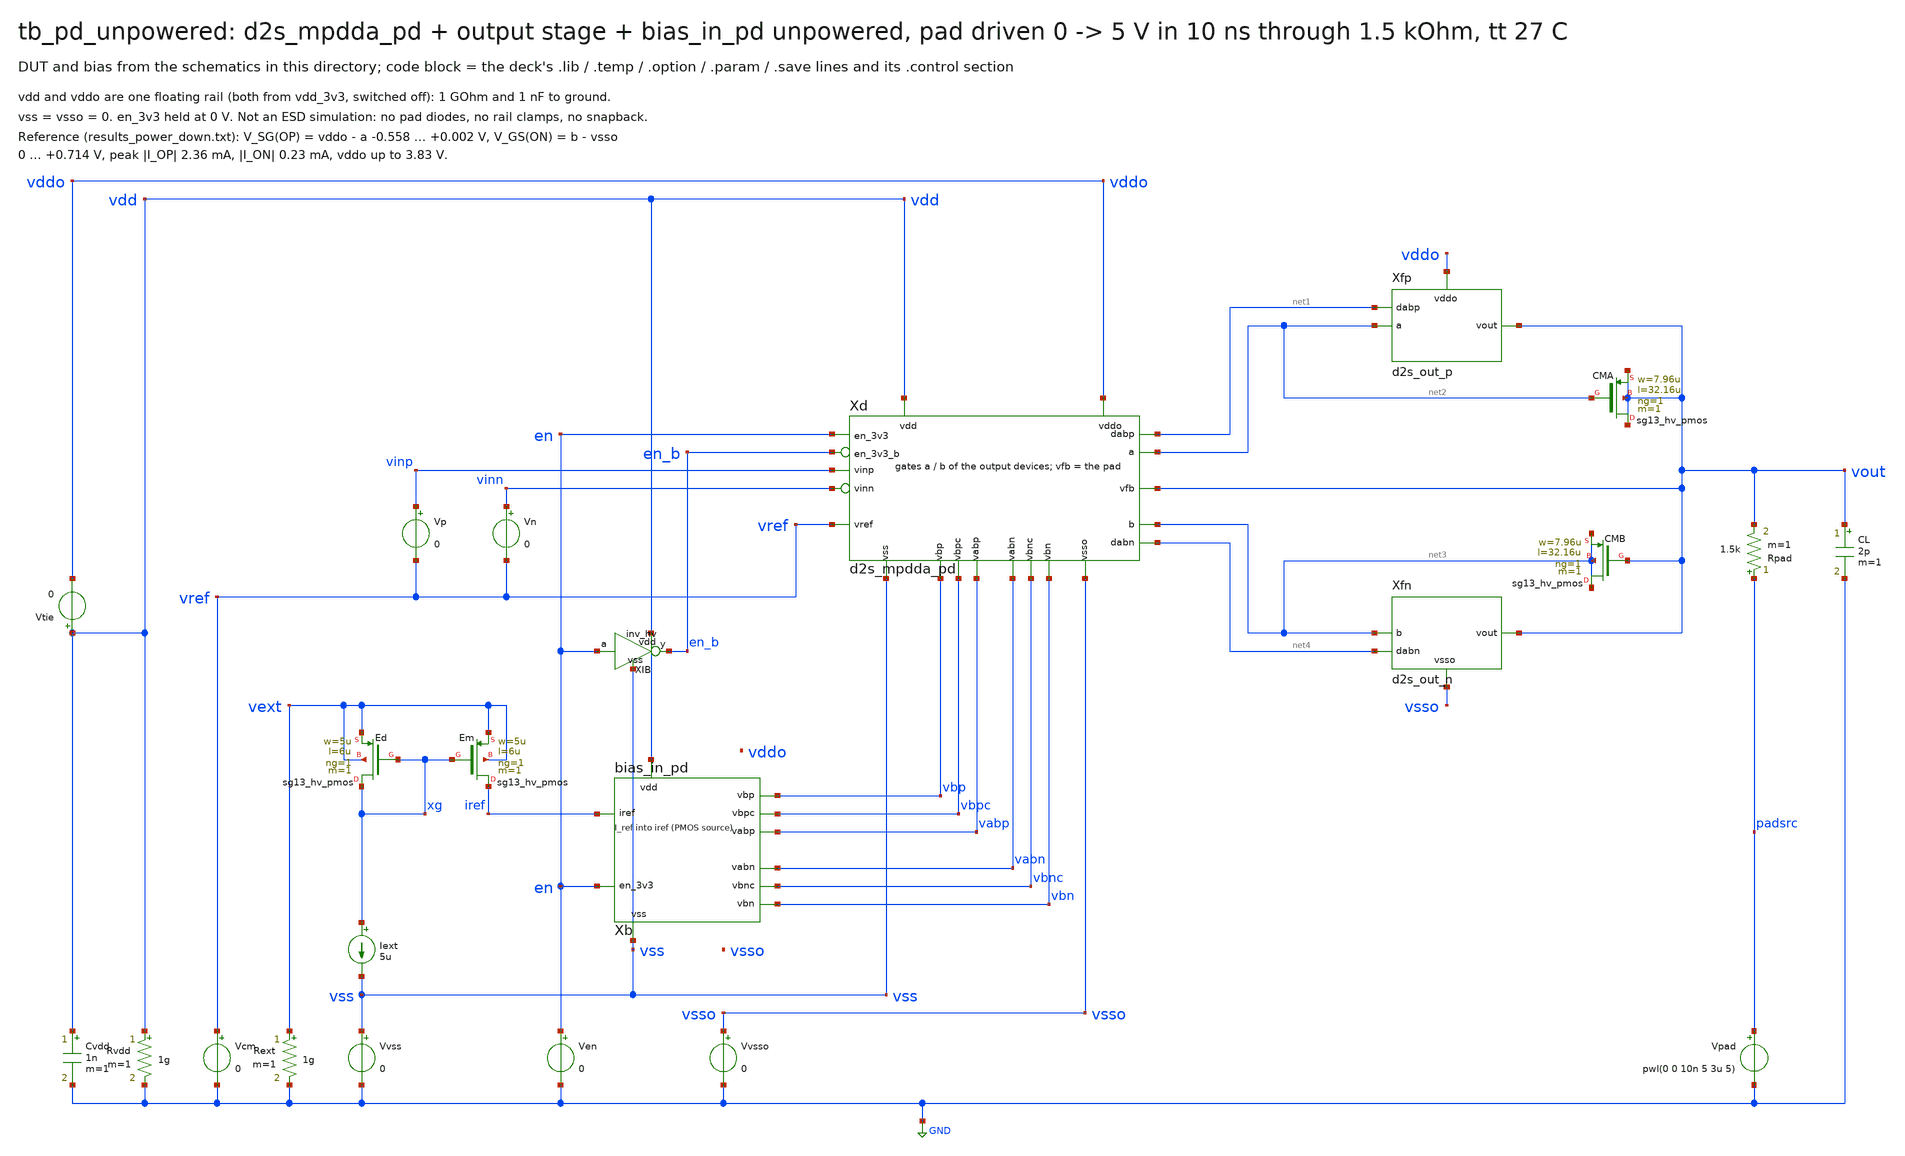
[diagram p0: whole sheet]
** sch_path: macros/sg13cmos5l_IOPadDiff2Single/testbenches/xschem/tb_pd_unpowered.sch
**.subckt tb_pd_unpowered
Vvss vss GND 0
Vvsso vsso GND 0
Ven en GND 0
Vcm vref GND 0
Xb vdd vss iref vbp vbn vbpc vbnc vabp vabn en bias_in_pd
Xd vdd vss vddo vsso vinp vinn vref vout net2 net3 net1 net4 vbp vbn vbpc vbnc vabp vabn en en_b
+ d2s_mpdda_pd
Vp vinp vref 0
Vn vinn vref 0
XEd xg xg vext vext sg13_hv_pmos w=5u l=6u ng=1 m=1 mm_ok=1
XEm iref xg vext vext sg13_hv_pmos w=5u l=6u ng=1 m=1 mm_ok=1
Iext xg vss 5u
CL vout GND 2p m=1
Rvdd vdd GND 1g m=1
Cvdd vdd GND 1n m=1
Vtie vdd vddo 0
Rext vext GND 1g m=1
Rpad padsrc vout 1.5k m=1
Vpad padsrc GND pwl(0 0 10n 5 3u 5)
XIB vdd vss en en_b inv_hv
Xfp vddo net2 vout net1 d2s_out_p
Xfn vsso net3 vout net4 d2s_out_n
XCMA vout net2 vout vout sg13_hv_pmos w=7.96u l=32.16u ng=1 m=1 mm_ok=1
XCMB net3 vout net3 net3 sg13_hv_pmos w=7.96u l=32.16u ng=1 m=1 mm_ok=1
**** begin user architecture code

.lib cornerMOShv.lib mos_tt
.lib cornerRES.lib res_typ
.lib cornerCAP.lib cap_typ
.temp 27
.option method=gear
.save v(vout) v(a) v(b) v(vddo) v(en_b) @n.xfp.xop.nsg13_hv_pmos[ids] @n.xfn.xon.nsg13_hv_nmos[ids]
.control
tran 1n 3u uic
let vsg_op = v(vddo) - v(a)
let vgs_on = v(b)
meas tran pmin min vsg_op
meas tran pmax max vsg_op
meas tran nmin min vgs_on
meas tran nmax max vgs_on
let ip = abs(@n.xfp.xop.nsg13_hv_pmos[ids])
let inn = abs(@n.xfn.xon.nsg13_hv_nmos[ids])
meas tran ipm max ip
meas tran inm max inn
meas tran vddm max v(vddo)
print pmin pmax nmin nmax ipm inm vddm
if $?batchmode = 0
  plot v(vout) v(vddo) v(a) v(b) v(en_b)
end
.endc

**** end user architecture code
**.ends
.GLOBAL GND
.end
